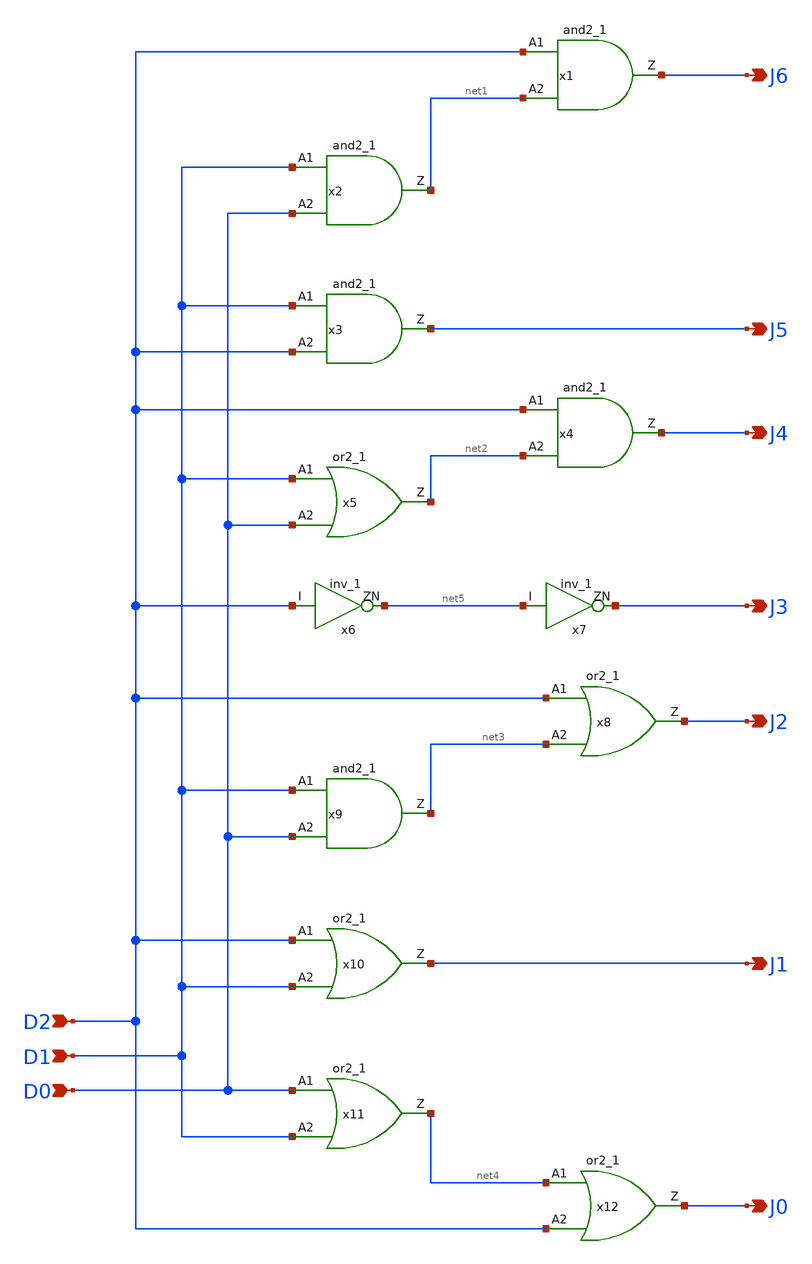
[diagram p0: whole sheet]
** sch_path: DAC/xschem/digital_cell/dac_decoder.sch
**.subckt dac_decoder J0 J1 J2 J3 J4 J5 J6 D2 D1 D0
*.opin J0
*.opin J1
*.opin J2
*.opin J3
*.opin J4
*.opin J5
*.opin J6
*.ipin D2
*.ipin D1
*.ipin D0
x1 D2 net1 J6 VDD VNW VPW VSS gf180mcu_fd_sc_mcu7t5v0__and2_1
x2 D1 D0 net1 VDD VNW VPW VSS gf180mcu_fd_sc_mcu7t5v0__and2_1
x3 D1 D2 J5 VDD VNW VPW VSS gf180mcu_fd_sc_mcu7t5v0__and2_1
x4 D2 net2 J4 VDD VNW VPW VSS gf180mcu_fd_sc_mcu7t5v0__and2_1
x5 D1 D0 net2 VDD VNW VPW VSS gf180mcu_fd_sc_mcu7t5v0__or2_1
x6 D2 net5 VDD VNW VPW VSS gf180mcu_fd_sc_mcu7t5v0__inv_1
x7 net5 J3 VDD VNW VPW VSS gf180mcu_fd_sc_mcu7t5v0__inv_1
x8 D2 net3 J2 VDD VNW VPW VSS gf180mcu_fd_sc_mcu7t5v0__or2_1
x9 D1 D0 net3 VDD VNW VPW VSS gf180mcu_fd_sc_mcu7t5v0__and2_1
x10 D2 D1 J1 VDD VNW VPW VSS gf180mcu_fd_sc_mcu7t5v0__or2_1
x11 D0 D1 net4 VDD VNW VPW VSS gf180mcu_fd_sc_mcu7t5v0__or2_1
x12 net4 D2 J0 VDD VNW VPW VSS gf180mcu_fd_sc_mcu7t5v0__or2_1
**.ends
.end
